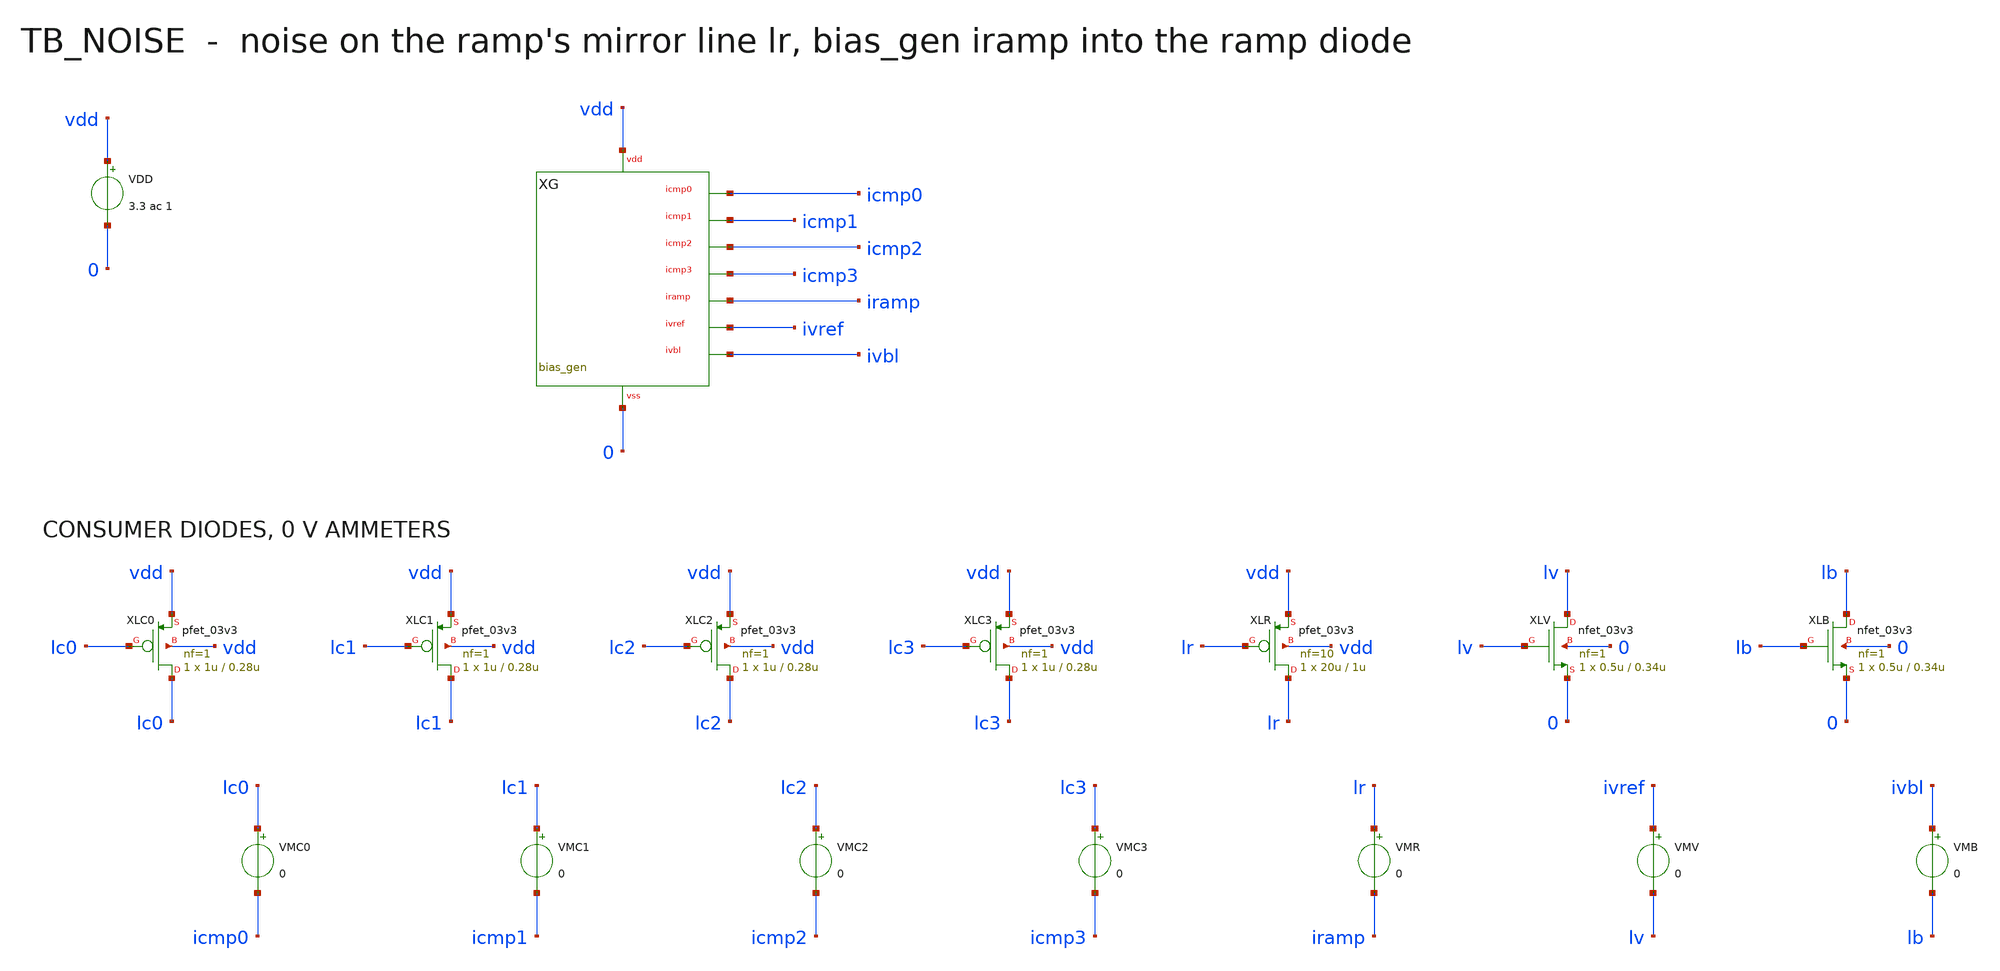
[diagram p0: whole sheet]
** sch_path: mixed_signal/bias_gen/tb_noise.sch
**.subckt tb_noise
VDD vdd 0 3.3 ac 1
XG vdd 0 icmp0 icmp1 icmp2 icmp3 iramp ivref ivbl bias_gen
XLC0 lc0 lc0 vdd vdd pfet_03v3 L=0.28u W=1u nf=1 m=1 ad=0.18p pd=2.36u as=0.18p ps=2.36u nrd=0.18
+ nrs=0.18
VMC0 lc0 icmp0 0
XLC1 lc1 lc1 vdd vdd pfet_03v3 L=0.28u W=1u nf=1 m=1 ad=0.18p pd=2.36u as=0.18p ps=2.36u nrd=0.18
+ nrs=0.18
VMC1 lc1 icmp1 0
XLC2 lc2 lc2 vdd vdd pfet_03v3 L=0.28u W=1u nf=1 m=1 ad=0.18p pd=2.36u as=0.18p ps=2.36u nrd=0.18
+ nrs=0.18
VMC2 lc2 icmp2 0
XLC3 lc3 lc3 vdd vdd pfet_03v3 L=0.28u W=1u nf=1 m=1 ad=0.18p pd=2.36u as=0.18p ps=2.36u nrd=0.18
+ nrs=0.18
VMC3 lc3 icmp3 0
XLR lr lr vdd vdd pfet_03v3 L=1u W=20u nf=10 m=1 ad=1.8p pd=21.8u as=2.16p ps=26.16u nrd=0.009
+ nrs=0.009
VMR lr iramp 0
XLV lv lv 0 0 nfet_03v3 L=0.34u W=0.5u nf=1 m=1 ad=0.09p pd=1.36u as=0.09p ps=1.36u nrd=0.36
+ nrs=0.36
VMV ivref lv 0
XLB lb lb 0 0 nfet_03v3 L=0.34u W=0.5u nf=1 m=1 ad=0.09p pd=1.36u as=0.09p ps=1.36u nrd=0.36
+ nrs=0.36
VMB ivbl lb 0
**** begin user architecture code

.include /foss/pdks/gf180mcuD/libs.tech/ngspice/design.ngspice
.lib /foss/pdks/gf180mcuD/libs.tech/ngspice/sm141064.ngspice typical
.lib /foss/pdks/gf180mcuD/libs.tech/ngspice/sm141064.ngspice res_typical
.lib /foss/pdks/gf180mcuD/libs.tech/ngspice/sm141064.ngspice mimcap_typical
.temp 27
.control
set num_threads=1
noise v(lr) VDD dec 20 1 100meg
setplot noise1
wrdata nz_new.txt onoise_spectrum
quit
.endc

**** end user architecture code
**.ends
.end
